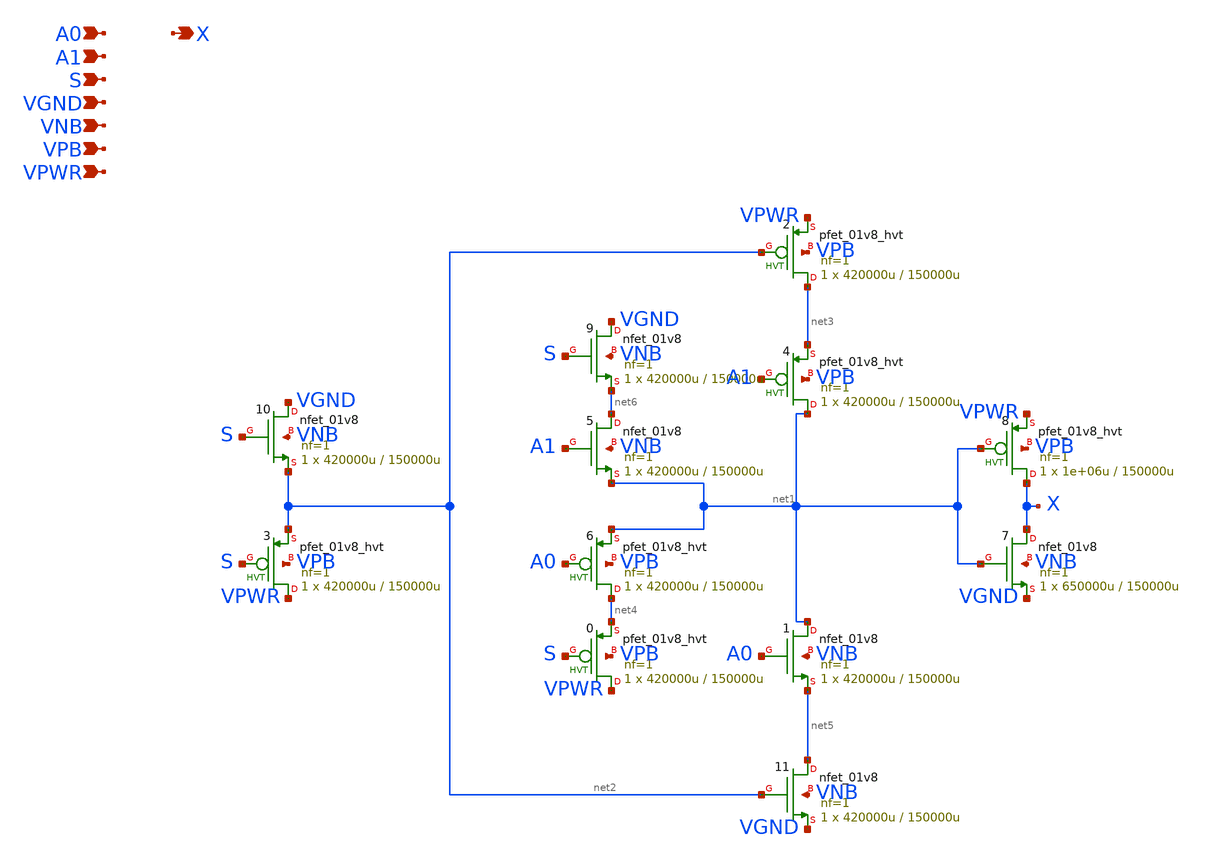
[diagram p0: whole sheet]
** sch_path: schematics/mux2/sky130_fd_sc_hd__mux2_1.sch
**.subckt sky130_fd_sc_hd__mux2_1 A0 A1 S VGND VNB VPB VPWR X
*.ipin A0
*.ipin A1
*.ipin S
*.ipin VGND
*.ipin VNB
*.ipin VPB
*.ipin VPWR
*.opin X
X7 X net1 VGND VNB sky130_fd_pr__nfet_01v8 L=150000u W=650000u nf=1 ad='int((1 + 1)/2) * 650000u / 1 * 0.29'
+ as='int((1 + 2)/2) * 650000u / 1 * 0.29' pd='2*int((1 + 1)/2) * (650000u / 1 + 0.29)' ps='2*int((1 + 2)/2) * (650000u / 1 + 0.29)'
+ nrd='0.29 / 650000u ' nrs='0.29 / 650000u ' sa=0 sb=0 sd=0 mult=1 m=1
X8 X net1 VPWR VPB sky130_fd_pr__pfet_01v8_hvt L=150000u W=1e+06u nf=1 ad='int((1 + 1)/2) * 1e+06u / 1 * 0.29'
+ as='int((1 + 2)/2) * 1e+06u / 1 * 0.29' pd='2*int((1 + 1)/2) * (1e+06u / 1 + 0.29)' ps='2*int((1 + 2)/2) * (1e+06u / 1 + 0.29)'
+ nrd='0.29 / 1e+06u ' nrs='0.29 / 1e+06u ' sa=0 sb=0 sd=0 mult=1 m=1
X1 net1 A0 net5 VNB sky130_fd_pr__nfet_01v8 L=150000u W=420000u nf=1 ad='int((nf+1)/2) * W/nf * 0.29'
+ as='int((nf+2)/2) * W/nf * 0.29' pd='2*int((nf+1)/2) * (W/nf + 0.29)' ps='2*int((nf+2)/2) * (W/nf + 0.29)'
+ nrd='0.29 / W' nrs='0.29 / W' sa=0 sb=0 sd=0 mult=1 m=1
X4 net1 A1 net3 VPB sky130_fd_pr__pfet_01v8_hvt L=150000u W=420000u nf=1 ad='int((nf+1)/2) * W/nf * 0.29'
+ as='int((nf+2)/2) * W/nf * 0.29' pd='2*int((nf+1)/2) * (W/nf + 0.29)' ps='2*int((nf+2)/2) * (W/nf + 0.29)'
+ nrd='0.29 / W' nrs='0.29 / W' sa=0 sb=0 sd=0 mult=1 m=1
X11 net5 net2 VGND VNB sky130_fd_pr__nfet_01v8 L=150000u W=420000u nf=1 ad='int((nf+1)/2) * W/nf * 0.29'
+ as='int((nf+2)/2) * W/nf * 0.29' pd='2*int((nf+1)/2) * (W/nf + 0.29)' ps='2*int((nf+2)/2) * (W/nf + 0.29)'
+ nrd='0.29 / W' nrs='0.29 / W' sa=0 sb=0 sd=0 mult=1 m=1
X2 net3 net2 VPWR VPB sky130_fd_pr__pfet_01v8_hvt L=150000u W=420000u nf=1 ad='int((nf+1)/2) * W/nf * 0.29'
+ as='int((nf+2)/2) * W/nf * 0.29' pd='2*int((nf+1)/2) * (W/nf + 0.29)' ps='2*int((nf+2)/2) * (W/nf + 0.29)'
+ nrd='0.29 / W' nrs='0.29 / W' sa=0 sb=0 sd=0 mult=1 m=1
X10 VGND S net2 VNB sky130_fd_pr__nfet_01v8 L=150000u W=420000u nf=1 ad='int((nf+1)/2) * W/nf * 0.29'
+ as='int((nf+2)/2) * W/nf * 0.29' pd='2*int((nf+1)/2) * (W/nf + 0.29)' ps='2*int((nf+2)/2) * (W/nf + 0.29)'
+ nrd='0.29 / W' nrs='0.29 / W' sa=0 sb=0 sd=0 mult=1 m=1
X3 VPWR S net2 VPB sky130_fd_pr__pfet_01v8_hvt L=150000u W=420000u nf=1 ad='int((nf+1)/2) * W/nf * 0.29'
+ as='int((nf+2)/2) * W/nf * 0.29' pd='2*int((nf+1)/2) * (W/nf + 0.29)' ps='2*int((nf+2)/2) * (W/nf + 0.29)'
+ nrd='0.29 / W' nrs='0.29 / W' sa=0 sb=0 sd=0 mult=1 m=1
X9 VGND S net6 VNB sky130_fd_pr__nfet_01v8 L=150000u W=420000u nf=1 ad='int((nf+1)/2) * W/nf * 0.29'
+ as='int((nf+2)/2) * W/nf * 0.29' pd='2*int((nf+1)/2) * (W/nf + 0.29)' ps='2*int((nf+2)/2) * (W/nf + 0.29)'
+ nrd='0.29 / W' nrs='0.29 / W' sa=0 sb=0 sd=0 mult=1 m=1
X5 net6 A1 net1 VNB sky130_fd_pr__nfet_01v8 L=150000u W=420000u nf=1 ad='int((nf+1)/2) * W/nf * 0.29'
+ as='int((nf+2)/2) * W/nf * 0.29' pd='2*int((nf+1)/2) * (W/nf + 0.29)' ps='2*int((nf+2)/2) * (W/nf + 0.29)'
+ nrd='0.29 / W' nrs='0.29 / W' sa=0 sb=0 sd=0 mult=1 m=1
X0 VPWR S net4 VPB sky130_fd_pr__pfet_01v8_hvt L=150000u W=420000u nf=1 ad='int((1 + 1)/2) * 420000u / 1 * 0.29'
+ as='int((1 + 2)/2) * 420000u / 1 * 0.29' pd='2*int((1 + 1)/2) * (420000u / 1 + 0.29)' ps='2*int((1 + 2)/2) * (420000u / 1 + 0.29)'
+ nrd='0.29 / 420000u ' nrs='0.29 / 420000u ' sa=0 sb=0 sd=0 mult=1 m=1
X6 net4 A0 net1 VPB sky130_fd_pr__pfet_01v8_hvt L=150000u W=420000u nf=1 ad='int((1 + 1)/2) * 420000u / 1 * 0.29'
+ as='int((1 + 2)/2) * 420000u / 1 * 0.29' pd='2*int((1 + 1)/2) * (420000u / 1 + 0.29)' ps='2*int((1 + 2)/2) * (420000u / 1 + 0.29)'
+ nrd='0.29 / 420000u ' nrs='0.29 / 420000u ' sa=0 sb=0 sd=0 mult=1 m=1
**.ends
.end
